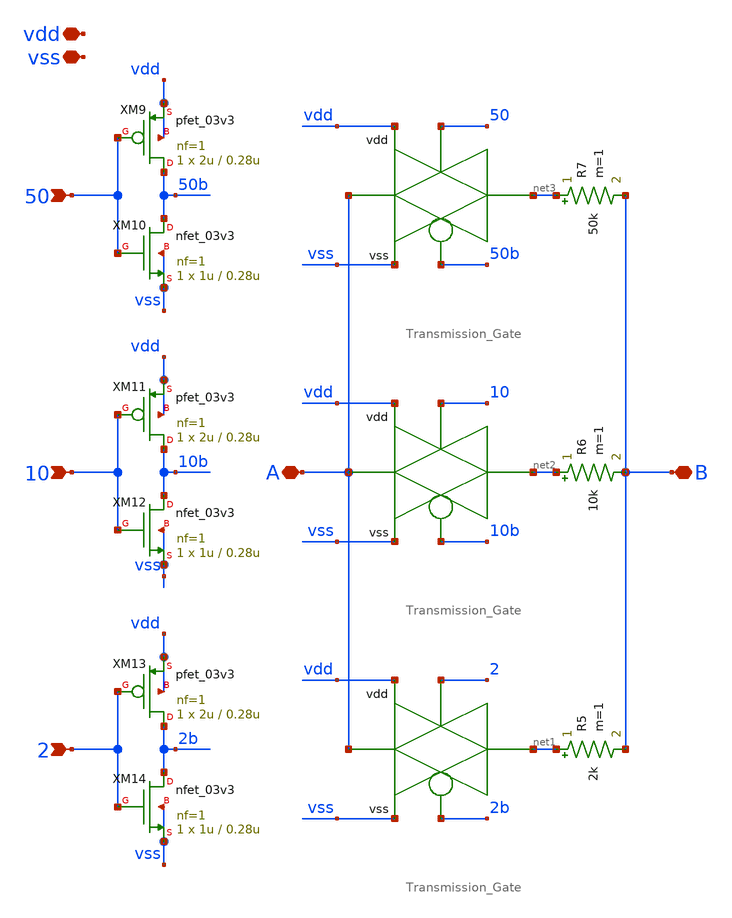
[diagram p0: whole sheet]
** sch_path: design/analog/PGA/gain_selector.sch
**.subckt gain_selector A B 2 10 50 vdd vss
*.iopin A
*.iopin B
*.ipin 2
*.ipin 10
*.ipin 50
*.iopin vdd
*.iopin vss
x9 A 2b 2 vdd vss net1 Transmission_Gate
R5 net1 B 2k m=1
x10 A 10b 10 vdd vss net2 Transmission_Gate
R6 net2 B 10k m=1
x11 A 50b 50 vdd vss net3 Transmission_Gate
R7 net3 B 50k m=1
XM9 50b 50 vdd vdd pfet_03v3 L=0.28u W=2u nf=1 ad='int((nf+1)/2) * W/nf * 0.18u' as='int((nf+2)/2) * W/nf * 0.18u'
+ pd='2*int((nf+1)/2) * (W/nf + 0.18u)' ps='2*int((nf+2)/2) * (W/nf + 0.18u)' nrd='0.18u / W' nrs='0.18u / W'
+ sa=0 sb=0 sd=0 m=1
XM10 50b 50 vss vss nfet_03v3 L=0.28u W=1u nf=1 ad='int((nf+1)/2) * W/nf * 0.18u' as='int((nf+2)/2) * W/nf * 0.18u'
+ pd='2*int((nf+1)/2) * (W/nf + 0.18u)' ps='2*int((nf+2)/2) * (W/nf + 0.18u)' nrd='0.18u / W' nrs='0.18u / W'
+ sa=0 sb=0 sd=0 m=1
XM11 10b 10 vdd vdd pfet_03v3 L=0.28u W=2u nf=1 ad='int((nf+1)/2) * W/nf * 0.18u' as='int((nf+2)/2) * W/nf * 0.18u'
+ pd='2*int((nf+1)/2) * (W/nf + 0.18u)' ps='2*int((nf+2)/2) * (W/nf + 0.18u)' nrd='0.18u / W' nrs='0.18u / W'
+ sa=0 sb=0 sd=0 m=1
XM12 10b 10 vss vss nfet_03v3 L=0.28u W=1u nf=1 ad='int((nf+1)/2) * W/nf * 0.18u' as='int((nf+2)/2) * W/nf * 0.18u'
+ pd='2*int((nf+1)/2) * (W/nf + 0.18u)' ps='2*int((nf+2)/2) * (W/nf + 0.18u)' nrd='0.18u / W' nrs='0.18u / W'
+ sa=0 sb=0 sd=0 m=1
XM13 2b 2 vdd vdd pfet_03v3 L=0.28u W=2u nf=1 ad='int((nf+1)/2) * W/nf * 0.18u' as='int((nf+2)/2) * W/nf * 0.18u'
+ pd='2*int((nf+1)/2) * (W/nf + 0.18u)' ps='2*int((nf+2)/2) * (W/nf + 0.18u)' nrd='0.18u / W' nrs='0.18u / W'
+ sa=0 sb=0 sd=0 m=1
XM14 2b 2 vss vss nfet_03v3 L=0.28u W=1u nf=1 ad='int((nf+1)/2) * W/nf * 0.18u' as='int((nf+2)/2) * W/nf * 0.18u'
+ pd='2*int((nf+1)/2) * (W/nf + 0.18u)' ps='2*int((nf+2)/2) * (W/nf + 0.18u)' nrd='0.18u / W' nrs='0.18u / W'
+ sa=0 sb=0 sd=0 m=1
**.ends

* expanding   symbol:  Transmission_Gate.sym # of pins=6
** sym_path: design/analog/transmission_gate/Transmission_Gate.sym
** sch_path: design/analog/transmission_gate/Transmission_Gate.sch
.subckt Transmission_Gate A en_b en vdd vss B
*.ipin en_b
*.iopin A
*.iopin B
*.ipin en
*.iopin vdd
*.iopin vss
XM1 B en_b A vdd pfet_03v3 L=0.28u W=20u nf=10 ad='int((nf+1)/2) * W/nf * 0.18u' as='int((nf+2)/2) * W/nf * 0.18u'
+ pd='2*int((nf+1)/2) * (W/nf + 0.18u)' ps='2*int((nf+2)/2) * (W/nf + 0.18u)' nrd='0.18u / W' nrs='0.18u / W'
+ sa=0 sb=0 sd=0 m=8
XM2 A en B vss nfet_03v3 L=0.28u W=10u nf=5 ad='int((nf+1)/2) * W/nf * 0.18u' as='int((nf+2)/2) * W/nf * 0.18u'
+ pd='2*int((nf+1)/2) * (W/nf + 0.18u)' ps='2*int((nf+2)/2) * (W/nf + 0.18u)' nrd='0.18u / W' nrs='0.18u / W'
+ sa=0 sb=0 sd=0 m=8
.ends

.end
